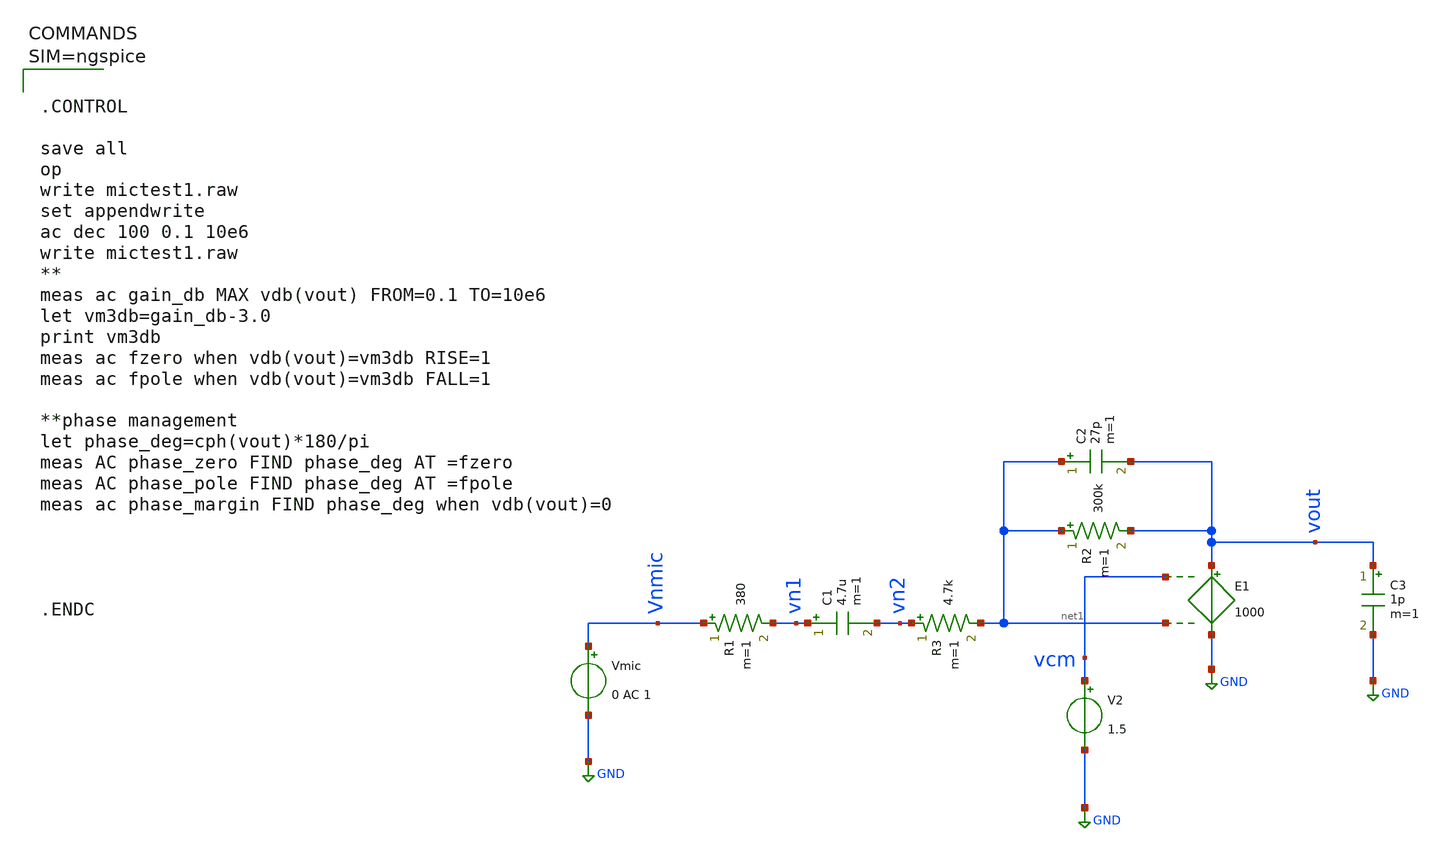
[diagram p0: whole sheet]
** sch_path: work/xschem/mictest1.sch
**.subckt mictest1
Vmic Vnmic GND 0 AC 1
R1 Vnmic vn1 380 m=1
C1 vn1 vn2 4.7u m=1
R3 vn2 net1 4.7k m=1
E1 vout GND vcm net1 1000
C2 net1 vout 27p m=1
R2 net1 vout 300k m=1
V2 vcm GND 1.5
C3 vout GND 1p m=1
**** begin user architecture code



.CONTROL

save all
op
write mictest1.raw
set appendwrite
ac dec 100 0.1 10e6
write mictest1.raw
**
meas ac gain_db MAX vdb(vout) FROM=0.1 TO=10e6
let vm3db=gain_db-3.0
print vm3db
meas ac fzero when vdb(vout)=vm3db RISE=1
meas ac fpole when vdb(vout)=vm3db FALL=1

**phase management
let phase_deg=cph(vout)*180/pi
meas AC phase_zero FIND phase_deg AT =fzero
meas AC phase_pole FIND phase_deg AT =fpole
meas ac phase_margin FIND phase_deg when vdb(vout)=0




.ENDC



**** end user architecture code
**.ends
.GLOBAL GND
.end
